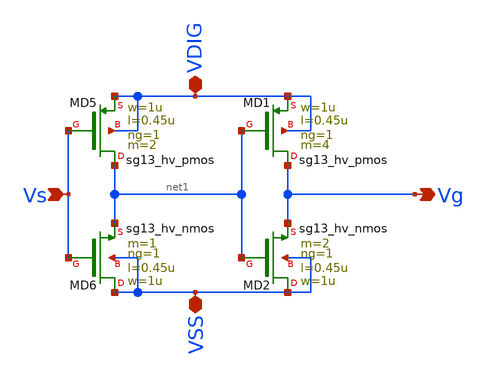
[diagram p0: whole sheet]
** sch_path: ChipUSM_AnalogTrack24/BUFFHVVCO/BUFFHVVCO_vto1p1.sch
**.subckt BUFFHVVCO_vto1p1 VDIG Vs Vg VSS
*.iopin VDIG
*.ipin Vs
*.opin Vg
*.iopin VSS
XMD5 net1 Vs VDIG VDIG sg13_hv_pmos w=1u l=0.45u ng=1 m=2 mm_ok=1
XMD6 VSS Vs net1 VSS sg13_hv_nmos w=1u l=0.45u ng=1 m=1 mm_ok=1
XMD1 Vg net1 VDIG VDIG sg13_hv_pmos w=1u l=0.45u ng=1 m=4 mm_ok=1
XMD2 VSS net1 Vg VSS sg13_hv_nmos w=1u l=0.45u ng=1 m=2 mm_ok=1
**.ends
.end
